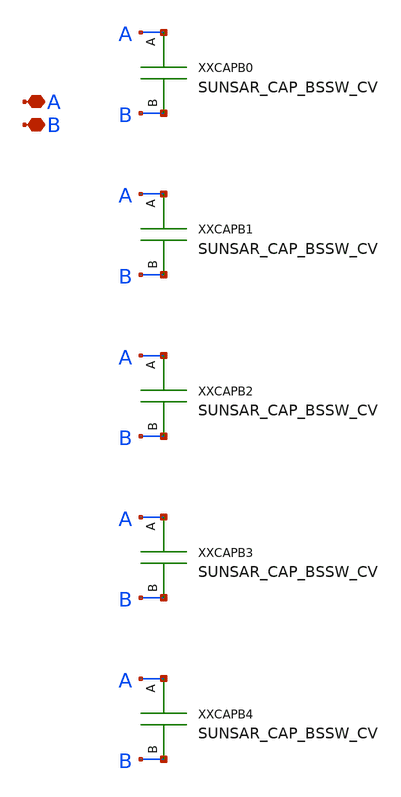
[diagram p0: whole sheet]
** sch_path: ip/sun_sar9b_sky130nm/design/SUN_SAR9B_SKY130NM/SUNSAR_CAP_BSSW5_CV.sch
**.subckt SUNSAR_CAP_BSSW5_CV A B
*.iopin A
*.iopin B
XXCAPB0 A B SUNSAR_CAP_BSSW_CV
XXCAPB1 A B SUNSAR_CAP_BSSW_CV
XXCAPB2 A B SUNSAR_CAP_BSSW_CV
XXCAPB3 A B SUNSAR_CAP_BSSW_CV
XXCAPB4 A B SUNSAR_CAP_BSSW_CV
**.ends

* expanding   symbol:  SUN_SAR9B_SKY130NM/SUNSAR_CAP_BSSW_CV.sym # of pins=2
** sym_path: ip/sun_sar9b_sky130nm/design/SUN_SAR9B_SKY130NM/SUNSAR_CAP_BSSW_CV.sym
** sch_path: ip/sun_sar9b_sky130nm/design/SUN_SAR9B_SKY130NM/SUNSAR_CAP_BSSW_CV.sch
.subckt SUNSAR_CAP_BSSW_CV A B
*.iopin A
*.iopin B
R1 A NC0 sky130_fd_pr__res_generic_m1 W=0.44 L=0.36 m=1
R2 B NC1 sky130_fd_pr__res_generic_m1 W=0.44 L=0.36 m=1
.ends

.end
